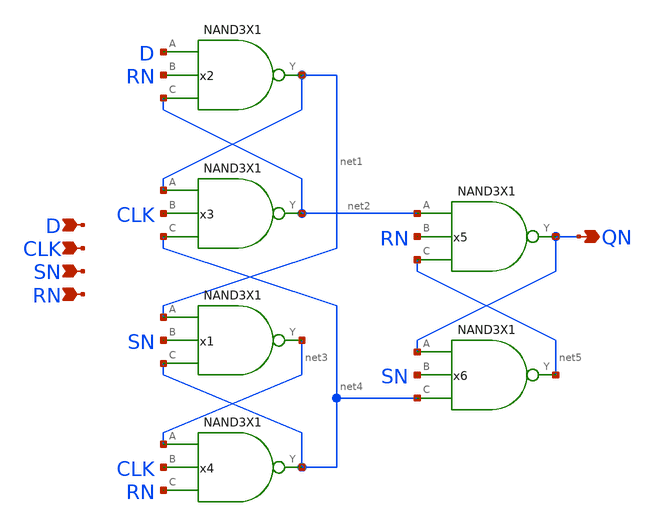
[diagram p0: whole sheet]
** sch_path: layout/xschem/sky130_rhbd/DFFSNRNQNX1.sch
**.subckt DFFSNRNQNX1 QN D CLK SN RN
*.opin QN
*.ipin D
*.ipin CLK
*.ipin SN
*.ipin RN
x1 net3 net1 SN net4 VDD VSS NAND3X1
x3 net2 net1 CLK net4 VDD VSS NAND3X1
x6 net5 QN SN net4 VDD VSS NAND3X1
x2 net1 D RN net2 VDD VSS NAND3X1
x4 net4 net3 CLK RN VDD VSS NAND3X1
x5 QN net2 RN net5 VDD VSS NAND3X1
**.ends
.end
